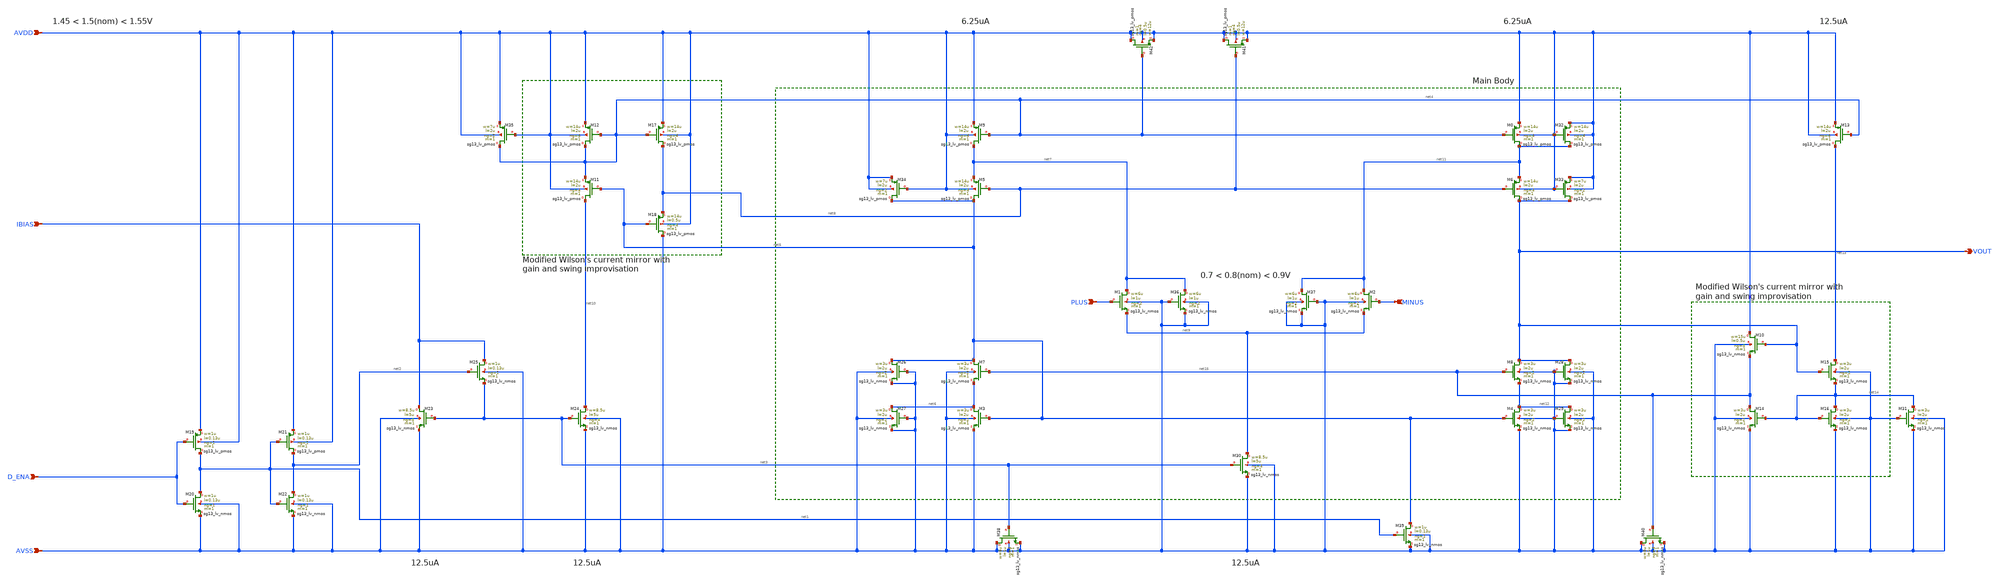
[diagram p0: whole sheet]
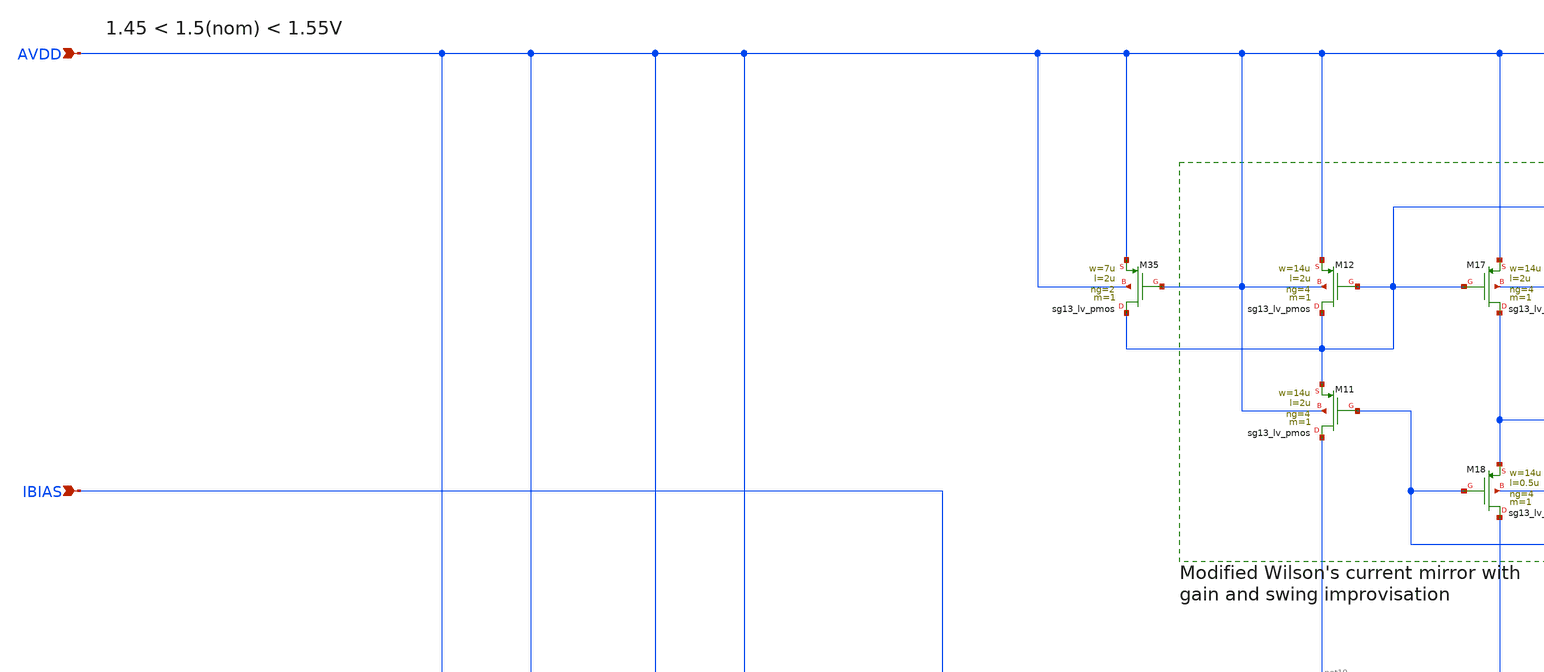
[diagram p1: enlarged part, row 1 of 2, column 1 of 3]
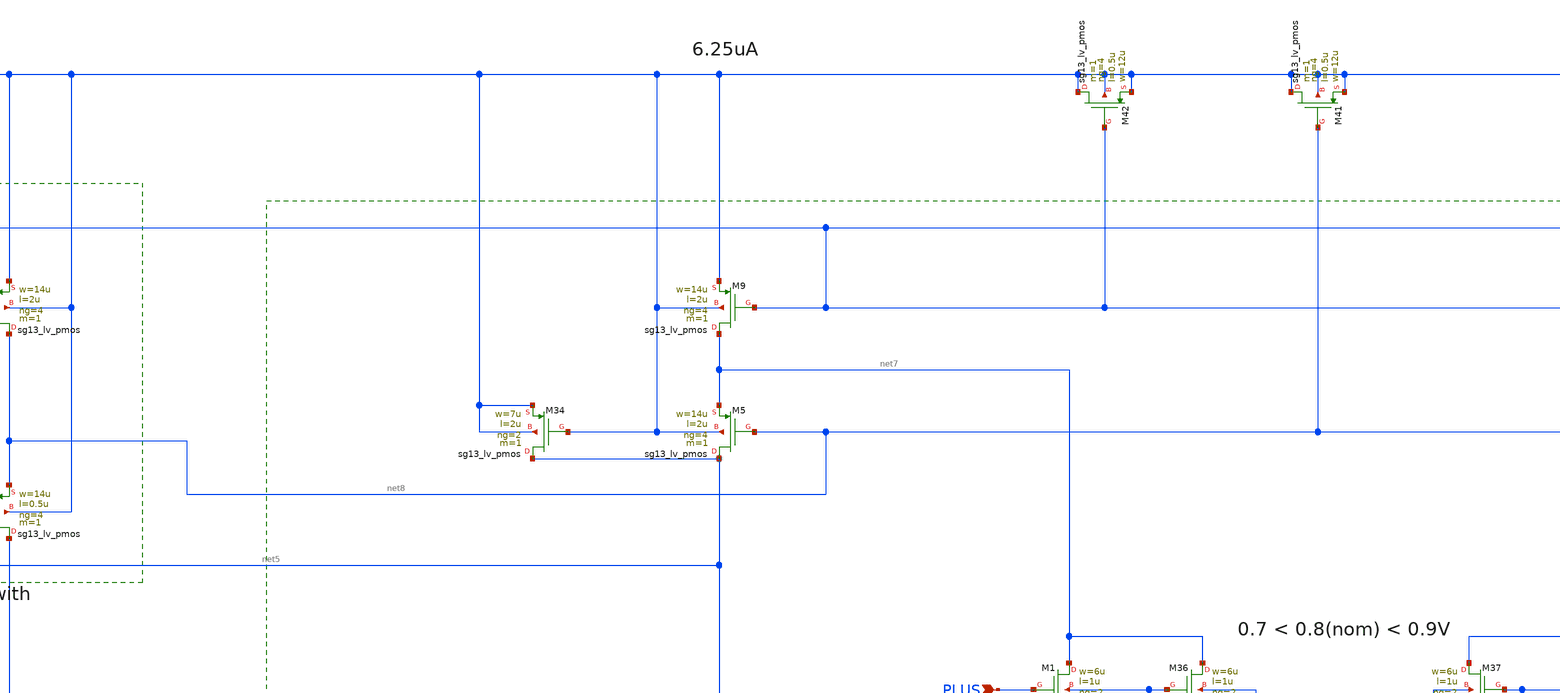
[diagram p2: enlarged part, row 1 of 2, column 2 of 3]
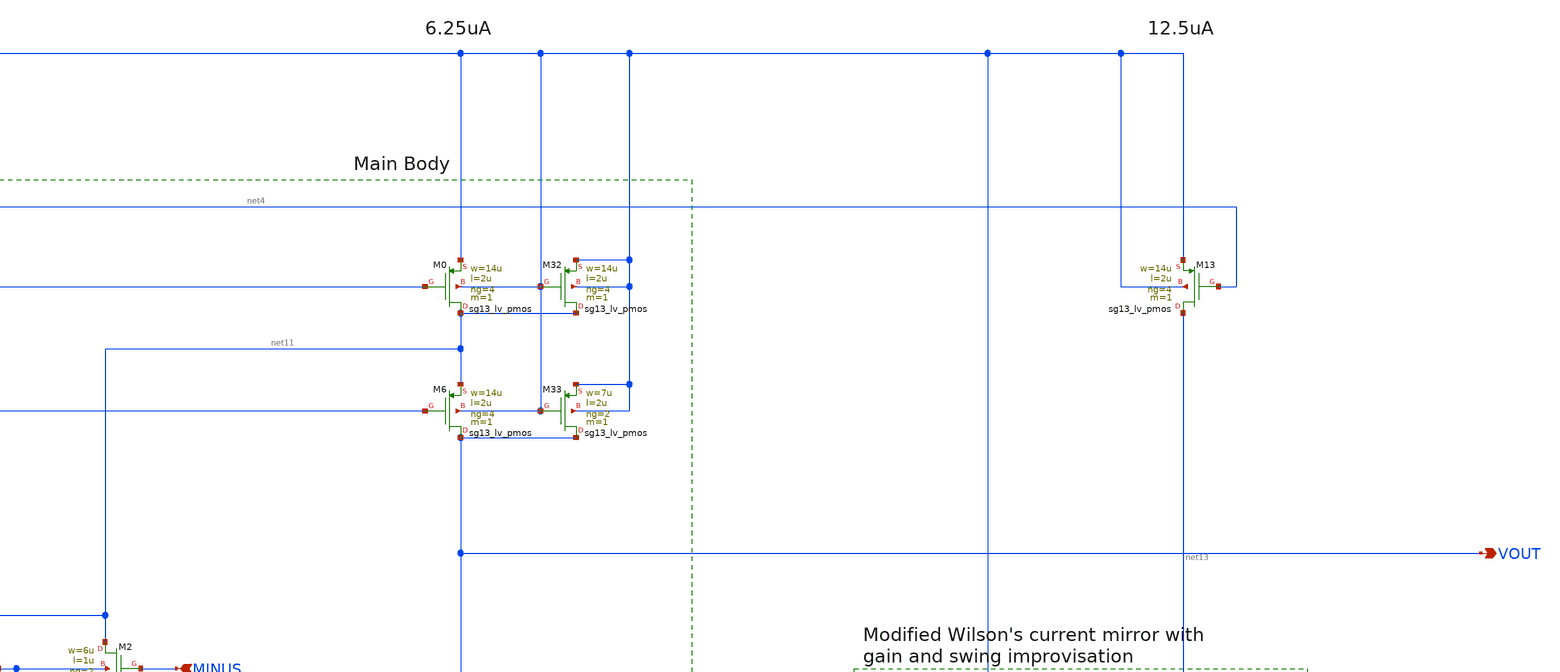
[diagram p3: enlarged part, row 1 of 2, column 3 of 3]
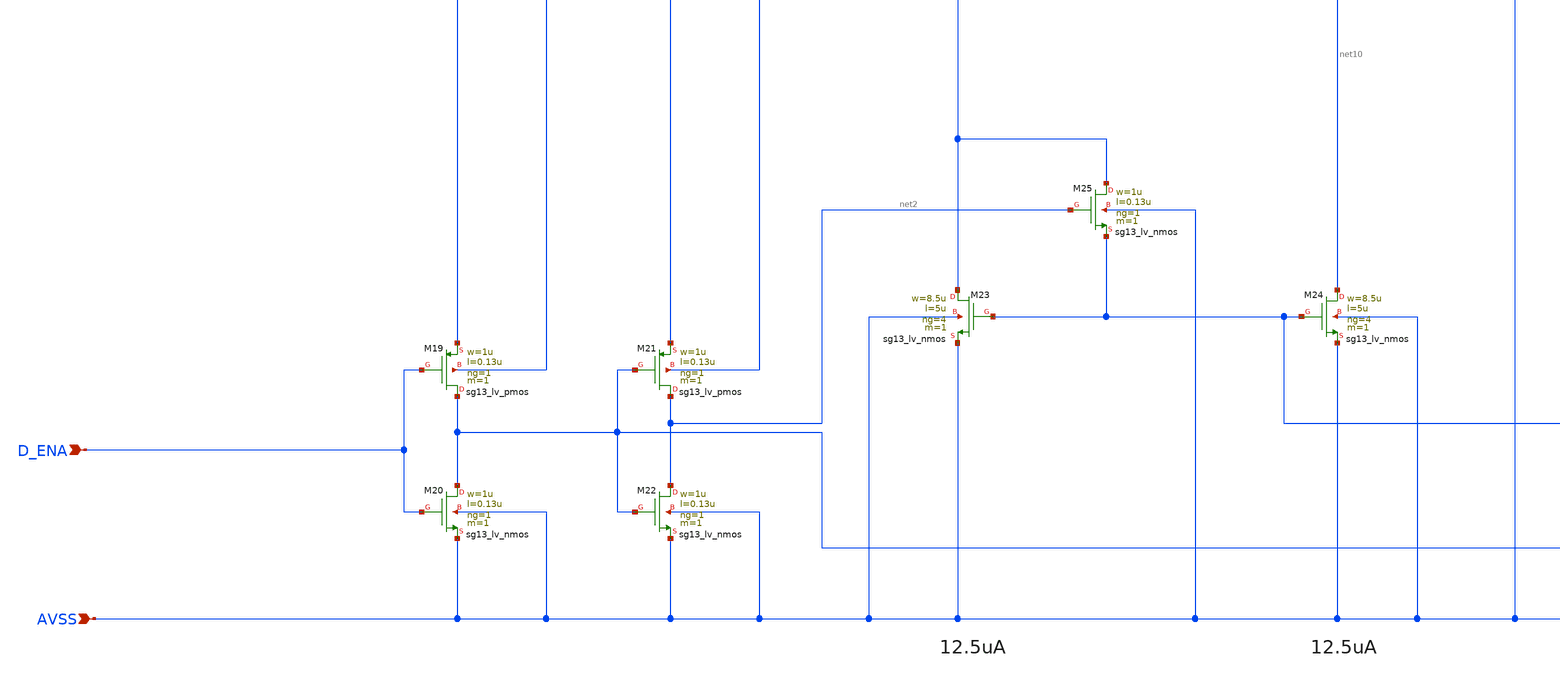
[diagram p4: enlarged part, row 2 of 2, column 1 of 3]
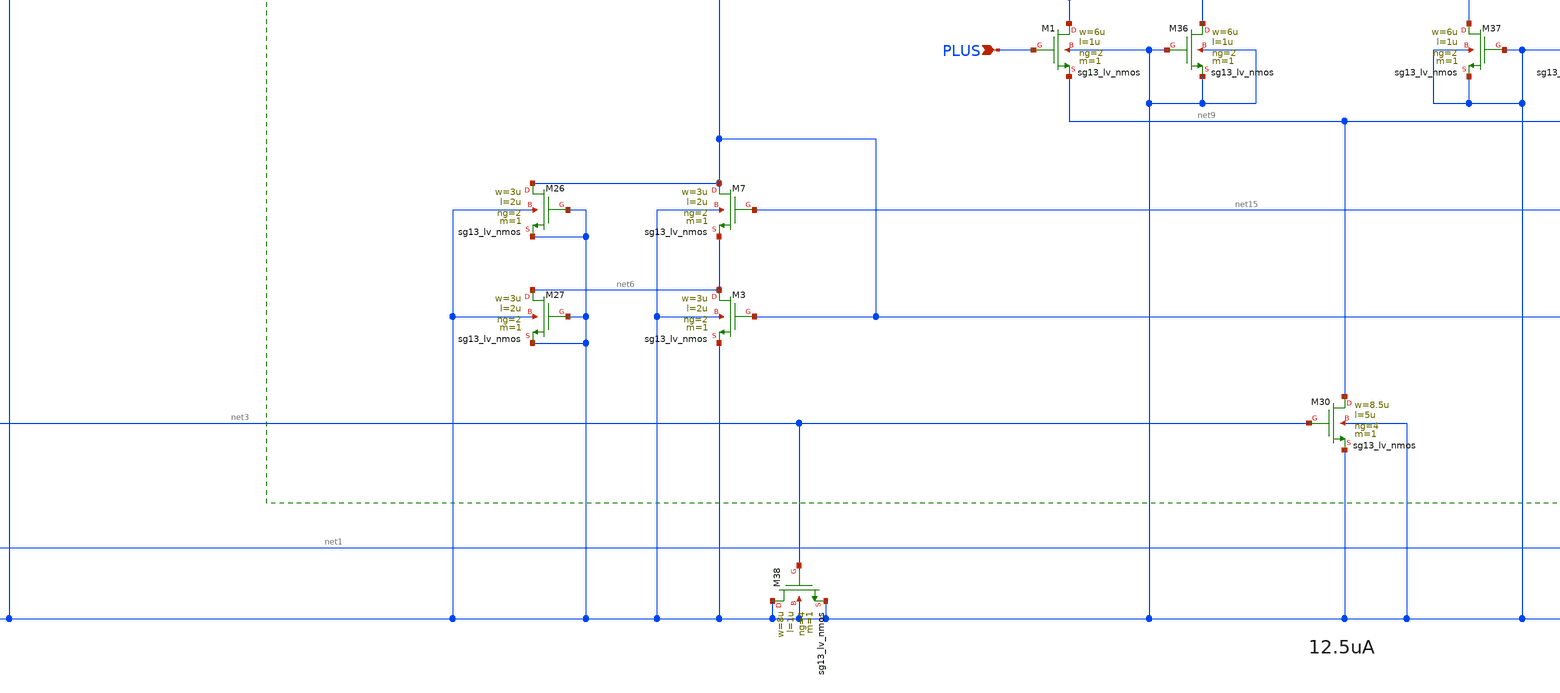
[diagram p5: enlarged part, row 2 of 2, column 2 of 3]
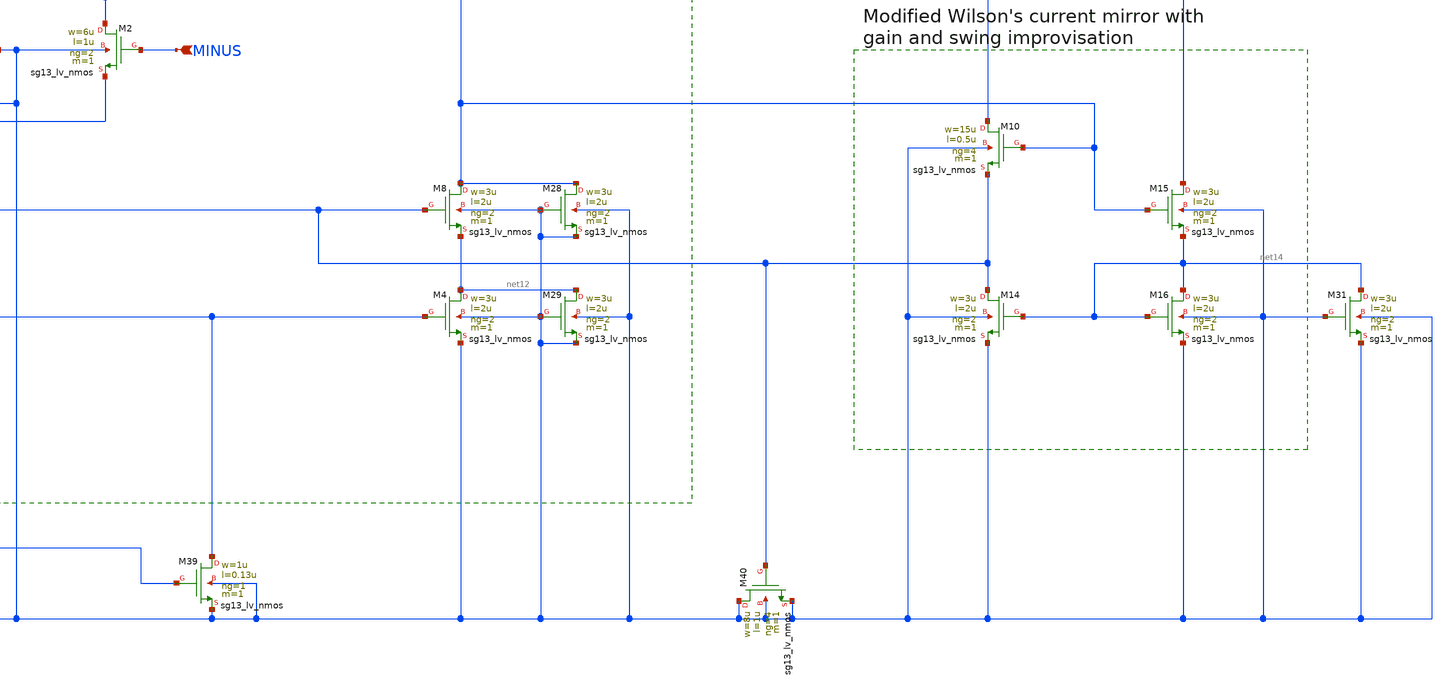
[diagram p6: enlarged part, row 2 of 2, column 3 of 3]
** sch_path: Designs/otas/1_schematics/foldedcascode_nmos_withdummies.sch
* (c) 2025 Thesis_HP, Apache-2.0 license
**.subckt foldedcascode_nmos_withdummies AVSS IBIAS AVDD PLUS MINUS VOUT D_ENA
*.ipin AVSS
*.ipin IBIAS
*.ipin AVDD
*.ipin PLUS
*.ipin MINUS
*.opin VOUT
*.ipin D_ENA
XM23 IBIAS net3 AVSS AVSS sg13_lv_nmos w=8.5u l=5u ng=4 m=1 mm_ok=1
XM25 IBIAS net2 net3 AVSS sg13_lv_nmos w=1u l=0.13u ng=1 m=1 mm_ok=1
XM24 net10 net3 AVSS AVSS sg13_lv_nmos w=8.5u l=5u ng=4 m=1 mm_ok=1
XM11 net10 net5 net4 AVDD sg13_lv_pmos w=14u l=2u ng=4 m=1 mm_ok=1
XM12 net4 net4 AVDD AVDD sg13_lv_pmos w=14u l=2u ng=4 m=1 mm_ok=1
XM18 AVSS net5 net8 AVDD sg13_lv_pmos w=14u l=0.5u ng=4 m=1 mm_ok=1
XM17 net8 net4 AVDD AVDD sg13_lv_pmos w=14u l=2u ng=4 m=1 mm_ok=1
XM9 net7 net4 AVDD AVDD sg13_lv_pmos w=14u l=2u ng=4 m=1 mm_ok=1
XM5 net5 net8 net7 AVDD sg13_lv_pmos w=14u l=2u ng=4 m=1 mm_ok=1
XM7 net5 net15 net6 AVSS sg13_lv_nmos w=3u l=2u ng=2 m=1 mm_ok=1
XM3 net6 net5 AVSS AVSS sg13_lv_nmos w=3u l=2u ng=2 m=1 mm_ok=1
XM30 net9 net3 AVSS AVSS sg13_lv_nmos w=8.5u l=5u ng=4 m=1 mm_ok=1
XM1 net7 PLUS net9 AVSS sg13_lv_nmos w=6u l=1u ng=2 m=1 mm_ok=1
XM2 net11 MINUS net9 AVSS sg13_lv_nmos w=6u l=1u ng=2 m=1 mm_ok=1
XM42 AVDD net4 AVDD AVDD sg13_lv_pmos w=12u l=0.5u ng=4 m=1 mm_ok=1
XM41 AVDD net8 AVDD AVDD sg13_lv_pmos w=12u l=0.5u ng=4 m=1 mm_ok=1
XM38 AVSS net3 AVSS AVSS sg13_lv_nmos w=8u l=1u ng=4 m=1 mm_ok=1
XM19 net1 D_ENA AVDD AVDD sg13_lv_pmos w=1u l=0.13u ng=1 m=1 mm_ok=1
XM21 net2 net1 AVDD AVDD sg13_lv_pmos w=1u l=0.13u ng=1 m=1 mm_ok=1
XM20 net1 D_ENA AVSS AVSS sg13_lv_nmos w=1u l=0.13u ng=1 m=1 mm_ok=1
XM22 net2 net1 AVSS AVSS sg13_lv_nmos w=1u l=0.13u ng=1 m=1 mm_ok=1
XM37 net11 AVSS AVSS AVSS sg13_lv_nmos w=6u l=1u ng=2 m=1 mm_ok=1
XM6 VOUT net8 net11 AVDD sg13_lv_pmos w=14u l=2u ng=4 m=1 mm_ok=1
XM0 net11 net4 AVDD AVDD sg13_lv_pmos w=14u l=2u ng=4 m=1 mm_ok=1
XM8 VOUT net15 net12 AVSS sg13_lv_nmos w=3u l=2u ng=2 m=1 mm_ok=1
XM4 net12 net5 AVSS AVSS sg13_lv_nmos w=3u l=2u ng=2 m=1 mm_ok=1
XM29 net12 AVSS AVSS AVSS sg13_lv_nmos w=3u l=2u ng=2 m=1 mm_ok=1
XM28 VOUT AVSS AVSS AVSS sg13_lv_nmos w=3u l=2u ng=2 m=1 mm_ok=1
XM32 net11 AVDD AVDD AVDD sg13_lv_pmos w=14u l=2u ng=4 m=1 mm_ok=1
XM33 VOUT AVDD AVDD AVDD sg13_lv_pmos w=7u l=2u ng=2 m=1 mm_ok=1
XM13 net13 net4 AVDD AVDD sg13_lv_pmos w=14u l=2u ng=4 m=1 mm_ok=1
XM15 net13 VOUT net14 AVSS sg13_lv_nmos w=3u l=2u ng=2 m=1 mm_ok=1
XM16 net14 net14 AVSS AVSS sg13_lv_nmos w=3u l=2u ng=2 m=1 mm_ok=1
XM14 net15 net14 AVSS AVSS sg13_lv_nmos w=3u l=2u ng=2 m=1 mm_ok=1
XM10 AVDD VOUT net15 AVSS sg13_lv_nmos w=15u l=0.5u ng=4 m=1 mm_ok=1
XM40 AVSS net15 AVSS AVSS sg13_lv_nmos w=8u l=1u ng=4 m=1 mm_ok=1
XM39 net5 net1 AVSS AVSS sg13_lv_nmos w=1u l=0.13u ng=1 m=1 mm_ok=1
XM36 net7 AVSS AVSS AVSS sg13_lv_nmos w=6u l=1u ng=2 m=1 mm_ok=1
XM34 net5 AVDD AVDD AVDD sg13_lv_pmos w=7u l=2u ng=2 m=1 mm_ok=1
XM27 net6 AVSS AVSS AVSS sg13_lv_nmos w=3u l=2u ng=2 m=1 mm_ok=1
XM26 net5 AVSS AVSS AVSS sg13_lv_nmos w=3u l=2u ng=2 m=1 mm_ok=1
XM35 net4 AVDD AVDD AVDD sg13_lv_pmos w=7u l=2u ng=2 m=1 mm_ok=1
XM31 net14 AVSS AVSS AVSS sg13_lv_nmos w=3u l=2u ng=2 m=1 mm_ok=1
**.ends
.end
